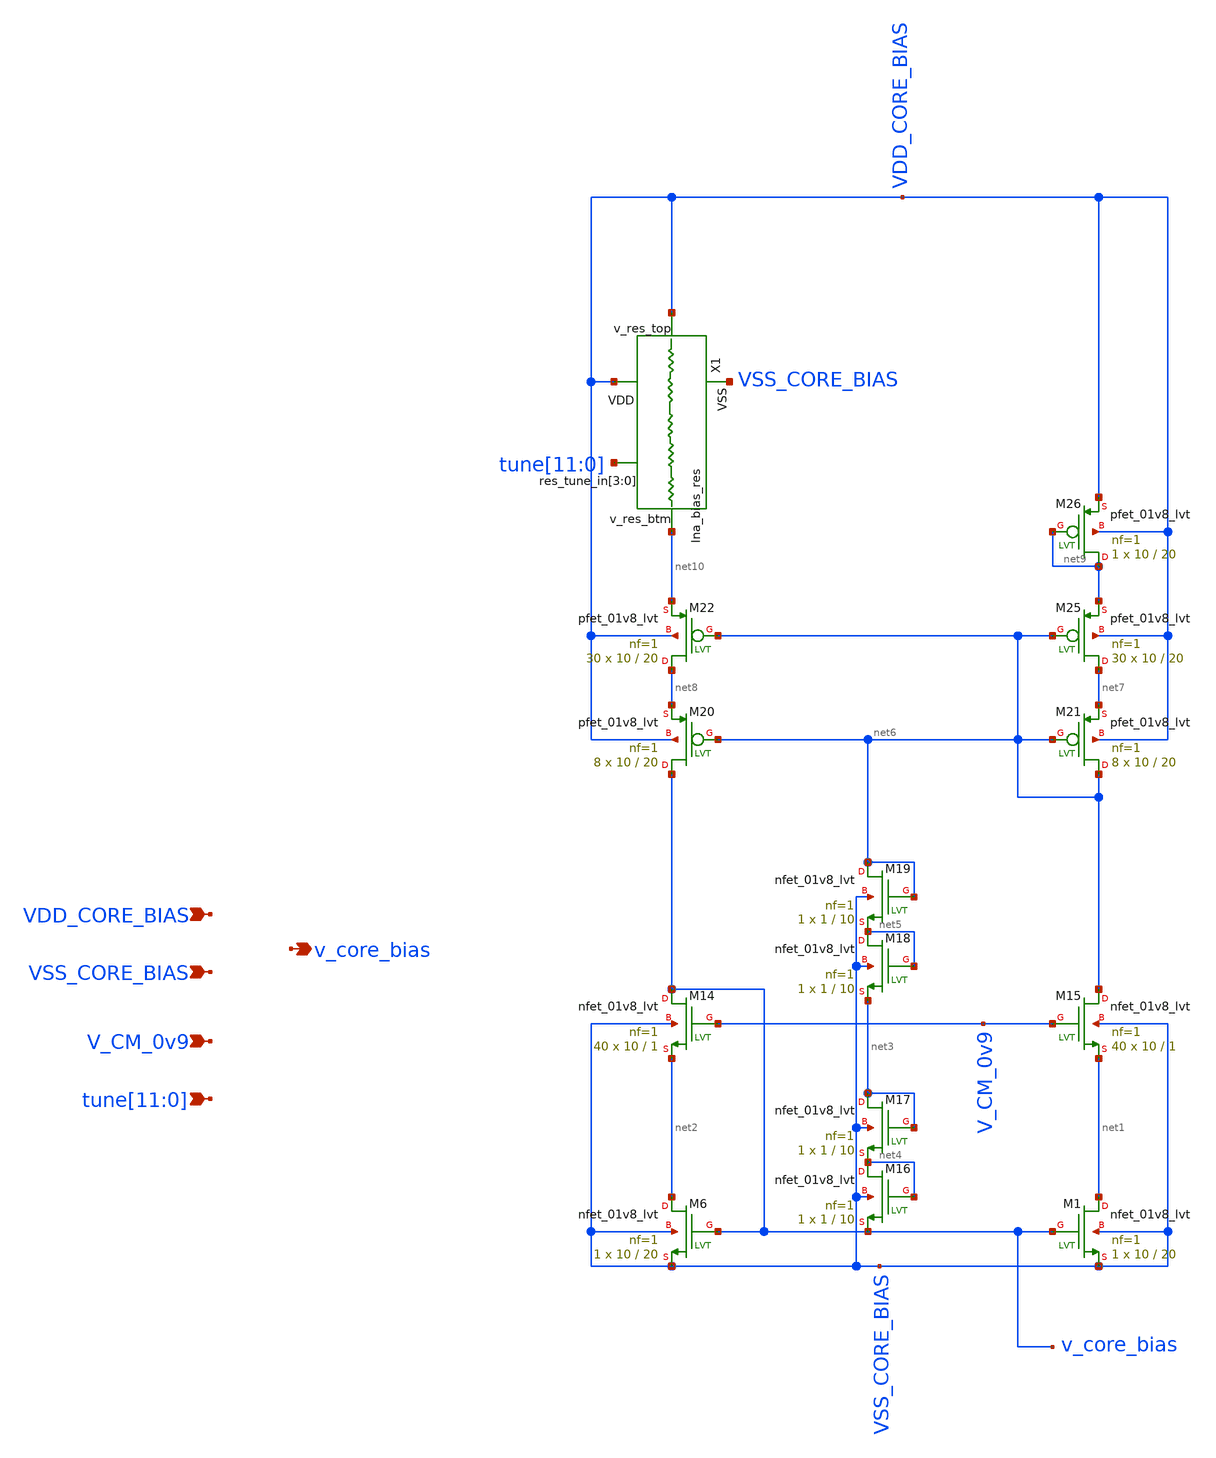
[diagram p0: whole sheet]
** sch_path: lna_bias.sch
**.subckt lna_bias VSS_CORE_BIAS VDD_CORE_BIAS v_core_bias V_CM_0v9
*+ tune[11],tune[10],tune[9],tune[8],tune[7],tune[6],tune[5],tune[4],tune[3],tune[2],tune[1],tune[0]
*.ipin VSS_CORE_BIAS
*.ipin VDD_CORE_BIAS
*.opin v_core_bias
*.ipin V_CM_0v9
*.ipin
*+ tune[11],tune[10],tune[9],tune[8],tune[7],tune[6],tune[5],tune[4],tune[3],tune[2],tune[1],tune[0]
XM1 net1 v_core_bias VSS_CORE_BIAS VSS_CORE_BIAS sky130_fd_pr__nfet_01v8_lvt L=20 W=10 nf=1 ad='int((nf+1)/2) * W/nf * 0.29'
+ as='int((nf+2)/2) * W/nf * 0.29' pd='2*int((nf+1)/2) * (W/nf + 0.29)' ps='2*int((nf+2)/2) * (W/nf + 0.29)'
+ nrd='0.29 / W' nrs='0.29 / W' sa=0 sb=0 sd=0 mult=1 m=1
XM6 net2 v_core_bias VSS_CORE_BIAS VSS_CORE_BIAS sky130_fd_pr__nfet_01v8_lvt L=20 W=10 nf=1 ad='int((nf+1)/2) * W/nf * 0.29'
+ as='int((nf+2)/2) * W/nf * 0.29' pd='2*int((nf+1)/2) * (W/nf + 0.29)' ps='2*int((nf+2)/2) * (W/nf + 0.29)'
+ nrd='0.29 / W' nrs='0.29 / W' sa=0 sb=0 sd=0 mult=1 m=1
XM14 v_core_bias V_CM_0v9 net2 VSS_CORE_BIAS sky130_fd_pr__nfet_01v8_lvt L=1 W=10 nf=1 ad='int((nf+1)/2) * W/nf * 0.29'
+ as='int((nf+2)/2) * W/nf * 0.29' pd='2*int((nf+1)/2) * (W/nf + 0.29)' ps='2*int((nf+2)/2) * (W/nf + 0.29)'
+ nrd='0.29 / W' nrs='0.29 / W' sa=0 sb=0 sd=0 mult=40 m=40
XM15 net6 V_CM_0v9 net1 VSS_CORE_BIAS sky130_fd_pr__nfet_01v8_lvt L=1 W=10 nf=1 ad='int((nf+1)/2) * W/nf * 0.29'
+ as='int((nf+2)/2) * W/nf * 0.29' pd='2*int((nf+1)/2) * (W/nf + 0.29)' ps='2*int((nf+2)/2) * (W/nf + 0.29)'
+ nrd='0.29 / W' nrs='0.29 / W' sa=0 sb=0 sd=0 mult=40 m=40
XM16 net4 net4 v_core_bias VSS_CORE_BIAS sky130_fd_pr__nfet_01v8_lvt L=10 W=1 nf=1 ad='int((nf+1)/2) * W/nf * 0.29'
+ as='int((nf+2)/2) * W/nf * 0.29' pd='2*int((nf+1)/2) * (W/nf + 0.29)' ps='2*int((nf+2)/2) * (W/nf + 0.29)'
+ nrd='0.29 / W' nrs='0.29 / W' sa=0 sb=0 sd=0 mult=1 m=1
XM17 net3 net3 net4 VSS_CORE_BIAS sky130_fd_pr__nfet_01v8_lvt L=10 W=1 nf=1 ad='int((nf+1)/2) * W/nf * 0.29'
+ as='int((nf+2)/2) * W/nf * 0.29' pd='2*int((nf+1)/2) * (W/nf + 0.29)' ps='2*int((nf+2)/2) * (W/nf + 0.29)'
+ nrd='0.29 / W' nrs='0.29 / W' sa=0 sb=0 sd=0 mult=1 m=1
XM18 net5 net5 net3 VSS_CORE_BIAS sky130_fd_pr__nfet_01v8_lvt L=10 W=1 nf=1 ad='int((nf+1)/2) * W/nf * 0.29'
+ as='int((nf+2)/2) * W/nf * 0.29' pd='2*int((nf+1)/2) * (W/nf + 0.29)' ps='2*int((nf+2)/2) * (W/nf + 0.29)'
+ nrd='0.29 / W' nrs='0.29 / W' sa=0 sb=0 sd=0 mult=1 m=1
XM19 net6 net6 net5 VSS_CORE_BIAS sky130_fd_pr__nfet_01v8_lvt L=10 W=1 nf=1 ad='int((nf+1)/2) * W/nf * 0.29'
+ as='int((nf+2)/2) * W/nf * 0.29' pd='2*int((nf+1)/2) * (W/nf + 0.29)' ps='2*int((nf+2)/2) * (W/nf + 0.29)'
+ nrd='0.29 / W' nrs='0.29 / W' sa=0 sb=0 sd=0 mult=1 m=1
XM20 v_core_bias net6 net8 VDD_CORE_BIAS sky130_fd_pr__pfet_01v8_lvt L=20 W=10 nf=1 ad='int((nf+1)/2) * W/nf * 0.29'
+ as='int((nf+2)/2) * W/nf * 0.29' pd='2*int((nf+1)/2) * (W/nf + 0.29)' ps='2*int((nf+2)/2) * (W/nf + 0.29)'
+ nrd='0.29 / W' nrs='0.29 / W' sa=0 sb=0 sd=0 mult=8 m=8
XM21 net6 net6 net7 VDD_CORE_BIAS sky130_fd_pr__pfet_01v8_lvt L=20 W=10 nf=1 ad='int((nf+1)/2) * W/nf * 0.29'
+ as='int((nf+2)/2) * W/nf * 0.29' pd='2*int((nf+1)/2) * (W/nf + 0.29)' ps='2*int((nf+2)/2) * (W/nf + 0.29)'
+ nrd='0.29 / W' nrs='0.29 / W' sa=0 sb=0 sd=0 mult=8 m=8
XM22 net8 net6 net10 VDD_CORE_BIAS sky130_fd_pr__pfet_01v8_lvt L=20 W=10 nf=1 ad='int((nf+1)/2) * W/nf * 0.29'
+ as='int((nf+2)/2) * W/nf * 0.29' pd='2*int((nf+1)/2) * (W/nf + 0.29)' ps='2*int((nf+2)/2) * (W/nf + 0.29)'
+ nrd='0.29 / W' nrs='0.29 / W' sa=0 sb=0 sd=0 mult=30 m=30
XM25 net7 net6 net9 VDD_CORE_BIAS sky130_fd_pr__pfet_01v8_lvt L=20 W=10 nf=1 ad='int((nf+1)/2) * W/nf * 0.29'
+ as='int((nf+2)/2) * W/nf * 0.29' pd='2*int((nf+1)/2) * (W/nf + 0.29)' ps='2*int((nf+2)/2) * (W/nf + 0.29)'
+ nrd='0.29 / W' nrs='0.29 / W' sa=0 sb=0 sd=0 mult=30 m=30
XM26 net9 net9 VDD_CORE_BIAS VDD_CORE_BIAS sky130_fd_pr__pfet_01v8_lvt L=20 W=10 nf=1 ad='int((nf+1)/2) * W/nf * 0.29'
+ as='int((nf+2)/2) * W/nf * 0.29' pd='2*int((nf+1)/2) * (W/nf + 0.29)' ps='2*int((nf+2)/2) * (W/nf + 0.29)'
+ nrd='0.29 / W' nrs='0.29 / W' sa=0 sb=0 sd=0 mult=1 m=1
X1 VSS_CORE_BIAS net10 VDD_CORE_BIAS VDD_CORE_BIAS tune[11] tune[10] tune[9] tune[8] tune[7] tune[6]
+ tune[5] tune[4] tune[3] tune[2] tune[1] tune[0] lna_bias_res
**.ends
.end
